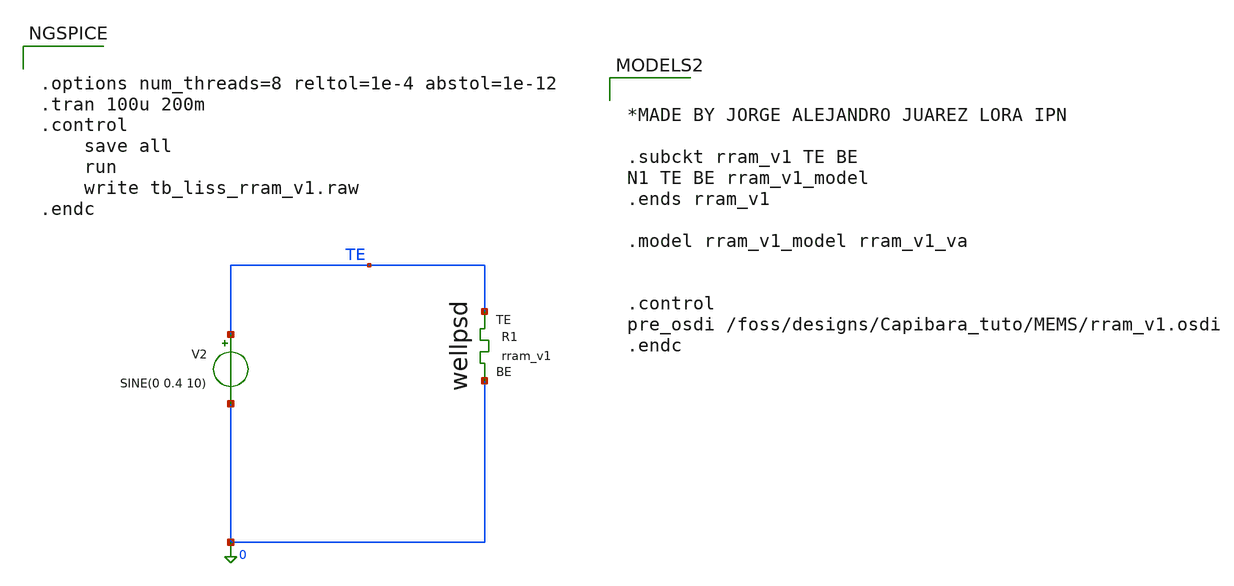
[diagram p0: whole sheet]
** sch_path: tb_liss_rram_v1.sch
**.subckt tb_liss_rram_v1
V2 TE 0 SINE(0 0.4 10)
XR1 TE 0 rram_v1
**** begin user architecture code


.options num_threads=8 reltol=1e-4 abstol=1e-12
.tran 100u 200m
.control
	save all
	run
	write tb_liss_rram_v1.raw
.endc




*MADE BY JORGE ALEJANDRO JUAREZ LORA IPN

.subckt rram_v1 TE BE
N1 TE BE rram_v1_model
.ends rram_v1

.model rram_v1_model rram_v1_va


.control
pre_osdi /foss/designs/Capibara_tuto/MEMS/rram_v1.osdi
.endc

**** end user architecture code
**.ends
.end
